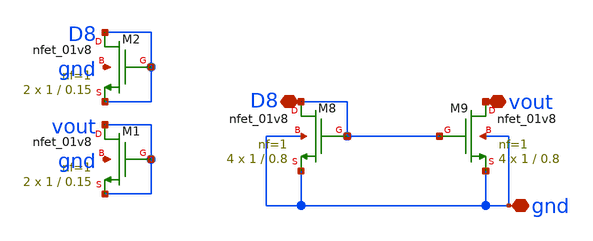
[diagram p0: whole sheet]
** sch_path: opamp/mag/nmosout.sch
**.subckt nmosout gnd vout D8
*.iopin gnd
*.iopin vout
*.iopin D8
XM9 vout D8 gnd gnd sky130_fd_pr__nfet_01v8 L=0.8 W=1 nf=1 ad='int((nf+1)/2) * W/nf * 0.29' as='int((nf+2)/2) * W/nf * 0.29'
+ pd='2*int((nf+1)/2) * (W/nf + 0.29)' ps='2*int((nf+2)/2) * (W/nf + 0.29)' nrd='0.29 / W' nrs='0.29 / W'
+ sa=0 sb=0 sd=0 mult=4 m=4
XM8 D8 D8 gnd gnd sky130_fd_pr__nfet_01v8 L=0.8 W=1 nf=1 ad='int((nf+1)/2) * W/nf * 0.29' as='int((nf+2)/2) * W/nf * 0.29'
+ pd='2*int((nf+1)/2) * (W/nf + 0.29)' ps='2*int((nf+2)/2) * (W/nf + 0.29)' nrd='0.29 / W' nrs='0.29 / W'
+ sa=0 sb=0 sd=0 mult=4 m=4
XM1 vout vout vout gnd sky130_fd_pr__nfet_01v8 L=0.15 W=1 nf=1 ad='int((nf+1)/2) * W/nf * 0.29' as='int((nf+2)/2) * W/nf * 0.29'
+ pd='2*int((nf+1)/2) * (W/nf + 0.29)' ps='2*int((nf+2)/2) * (W/nf + 0.29)' nrd='0.29 / W' nrs='0.29 / W'
+ sa=0 sb=0 sd=0 mult=2 m=2
XM2 D8 D8 D8 gnd sky130_fd_pr__nfet_01v8 L=0.15 W=1 nf=1 ad='int((nf+1)/2) * W/nf * 0.29' as='int((nf+2)/2) * W/nf * 0.29'
+ pd='2*int((nf+1)/2) * (W/nf + 0.29)' ps='2*int((nf+2)/2) * (W/nf + 0.29)' nrd='0.29 / W' nrs='0.29 / W'
+ sa=0 sb=0 sd=0 mult=2 m=2
**.ends
.end
